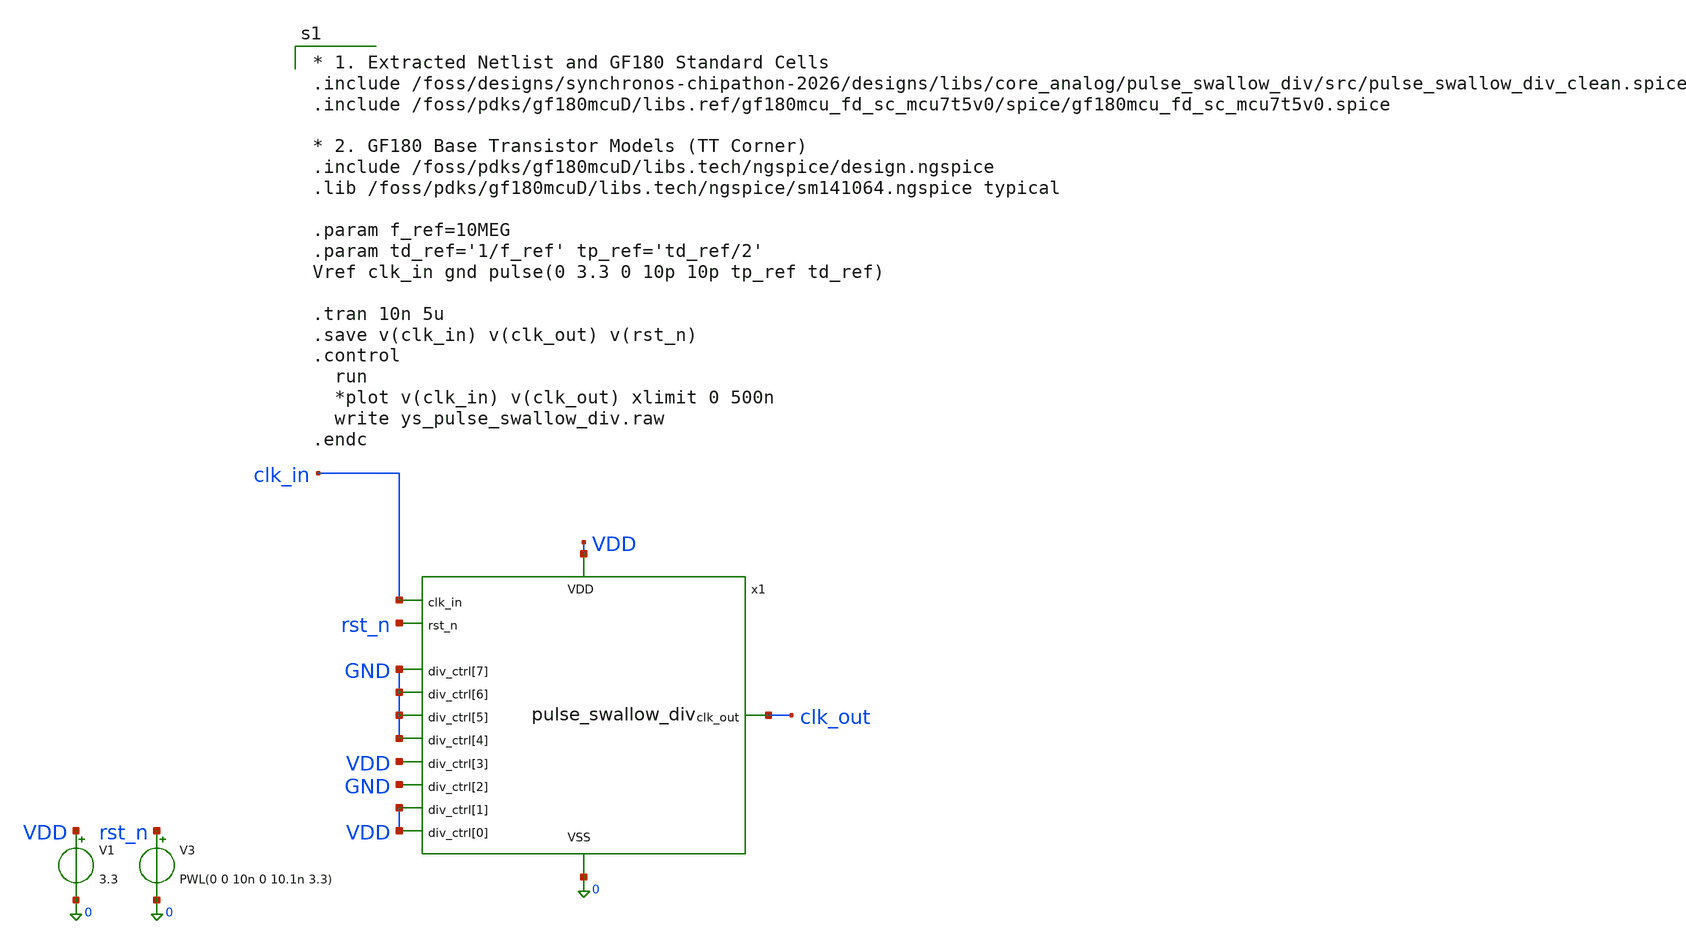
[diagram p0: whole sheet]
** sch_path: designs/libs/tb_analog/tb_pulse_swallow_div/ys_pulse_swallow_tb.sch
**.subckt ys_pulse_swallow_tb
V1 VDD 0 3.3
V3 rst_n 0 PWL(0 0 10n 0 10.1n 3.3)
x1 VDD 0 clk_in clk_out VDD VDD GND VDD GND GND GND GND rst_n pulse_swallow_div
**** begin user architecture code

* 1. Extracted Netlist and GF180 Standard Cells
.include /foss/designs/synchronos-chipathon-2026/designs/libs/core_analog/pulse_swallow_div/src/pulse_swallow_div_clean.spice
.include /foss/pdks/gf180mcuD/libs.ref/gf180mcu_fd_sc_mcu7t5v0/spice/gf180mcu_fd_sc_mcu7t5v0.spice

* 2. GF180 Base Transistor Models (TT Corner)
.include /foss/pdks/gf180mcuD/libs.tech/ngspice/design.ngspice
.lib /foss/pdks/gf180mcuD/libs.tech/ngspice/sm141064.ngspice typical

.param f_ref=10MEG
.param td_ref='1/f_ref' tp_ref='td_ref/2'
Vref clk_in gnd pulse(0 3.3 0 10p 10p tp_ref td_ref)

.tran 10n 5u
.save v(clk_in) v(clk_out) v(rst_n)
.control
  run
  *plot v(clk_in) v(clk_out) xlimit 0 500n
  write ys_pulse_swallow_div.raw
.endc

**** end user architecture code
**.ends
.end
